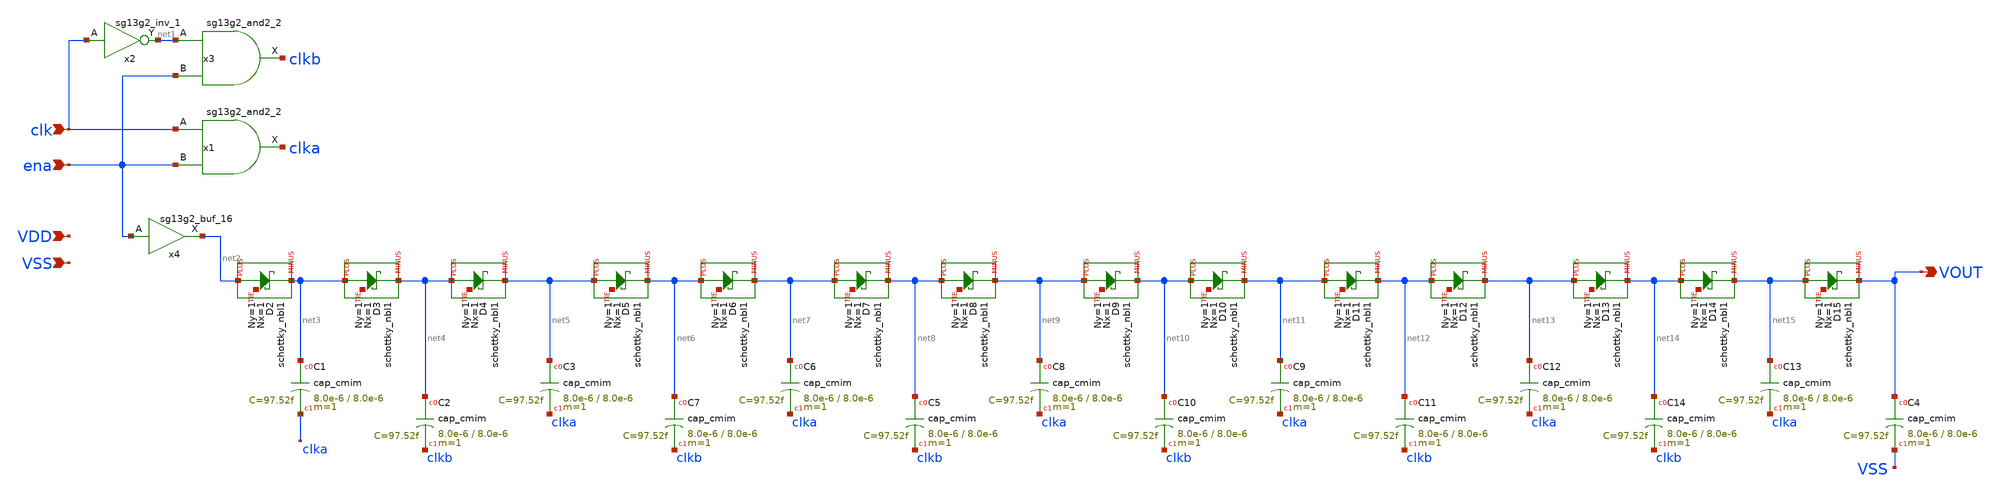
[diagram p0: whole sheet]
** sch_path: ihp130_cells/Schottky_PosChargePump/schottky_pump.sch
**.subckt schottky_pump clk ena VDD VSS VOUT
*.ipin clk
*.ipin ena
*.ipin VDD
*.ipin VSS
*.opin VOUT
XC1 net3 clka cap_cmim w=8.0e-6 l=8.0e-6 m=1 mm_ok=1
XC2 net4 clkb cap_cmim w=8.0e-6 l=8.0e-6 m=1 mm_ok=1
XC3 net5 clka cap_cmim w=8.0e-6 l=8.0e-6 m=1 mm_ok=1
XC4 VOUT VSS cap_cmim w=8.0e-6 l=8.0e-6 m=1 mm_ok=1
x1 clka clk ena VDD VSS sg13g2_and2_2
x2 net1 clk VDD VSS sg13g2_inv_1
x3 clkb net1 ena VDD VSS sg13g2_and2_2
x4 net2 ena VDD VSS sg13g2_buf_16
XC6 net7 clka cap_cmim w=8.0e-6 l=8.0e-6 m=1 mm_ok=1
XC7 net6 clkb cap_cmim w=8.0e-6 l=8.0e-6 m=1 mm_ok=1
XC5 net8 clkb cap_cmim w=8.0e-6 l=8.0e-6 m=1 mm_ok=1
XC8 net9 clka cap_cmim w=8.0e-6 l=8.0e-6 m=1 mm_ok=1
XC9 net11 clka cap_cmim w=8.0e-6 l=8.0e-6 m=1 mm_ok=1
XC10 net10 clkb cap_cmim w=8.0e-6 l=8.0e-6 m=1 mm_ok=1
XC11 net12 clkb cap_cmim w=8.0e-6 l=8.0e-6 m=1 mm_ok=1
XC12 net13 clka cap_cmim w=8.0e-6 l=8.0e-6 m=1 mm_ok=1
XC13 net15 clka cap_cmim w=8.0e-6 l=8.0e-6 m=1 mm_ok=1
XC14 net14 clkb cap_cmim w=8.0e-6 l=8.0e-6 m=1 mm_ok=1
XD2 net2 net3 net16 schottky_nbl1 Nx=1 Ny=1
XD3 net3 net4 net17 schottky_nbl1 Nx=1 Ny=1
XD4 net4 net5 net18 schottky_nbl1 Nx=1 Ny=1
XD5 net5 net6 net19 schottky_nbl1 Nx=1 Ny=1
XD6 net6 net7 net20 schottky_nbl1 Nx=1 Ny=1
XD7 net7 net8 net21 schottky_nbl1 Nx=1 Ny=1
XD8 net8 net9 net22 schottky_nbl1 Nx=1 Ny=1
XD9 net9 net10 net23 schottky_nbl1 Nx=1 Ny=1
XD10 net10 net11 net24 schottky_nbl1 Nx=1 Ny=1
XD11 net11 net12 net25 schottky_nbl1 Nx=1 Ny=1
XD12 net12 net13 net26 schottky_nbl1 Nx=1 Ny=1
XD13 net13 net14 net27 schottky_nbl1 Nx=1 Ny=1
XD14 net14 net15 net28 schottky_nbl1 Nx=1 Ny=1
XD15 net15 VOUT net29 schottky_nbl1 Nx=1 Ny=1
**.ends

* expanding   symbol:  sg13g2_stdcells/sg13g2_and2_2.sym # of pins=3
** sym_path: sg13g2_stdcells/sg13g2_and2_2.sym
** sch_path: sg13g2_stdcells/sg13g2_and2_2.sch
.subckt sg13g2_and2_2 X A B VDD VSS
*.ipin A
*.ipin B
*.opin X
*.iopin VDD
*.iopin VSS
XM1 net1 A net2 VSS sg13_lv_nmos w=640.00n l=130.00n ng=1 m=1 mm_ok=1
XM2 net2 B VSS VSS sg13_lv_nmos w=640.00n l=130.00n ng=1 m=1 mm_ok=1
XM3 X net1 VSS VSS sg13_lv_nmos w=1.48u l=130.00n ng=2 m=1 mm_ok=1
XM4 net1 B VDD VDD sg13_lv_pmos w=840.00n l=130.00n ng=1 m=1 mm_ok=1
XM5 net1 A VDD VDD sg13_lv_pmos w=840.00n l=130.00n ng=1 m=1 mm_ok=1
XM6 X net1 VDD VDD sg13_lv_pmos w=2.24u l=130.00n ng=2 m=1 mm_ok=1
.ends


* expanding   symbol:  sg13g2_stdcells/sg13g2_inv_1.sym # of pins=2
** sym_path: sg13g2_stdcells/sg13g2_inv_1.sym
** sch_path: sg13g2_stdcells/sg13g2_inv_1.sch
.subckt sg13g2_inv_1 Y A VDD VSS
*.opin Y
*.ipin A
*.iopin VDD
*.iopin VSS
XM1 Y A VSS VSS sg13_lv_nmos w=740.00n l=130.00n ng=1 m=1 mm_ok=1
XM2 Y A VDD VDD sg13_lv_pmos w=1.12u l=130.00n ng=1 m=1 mm_ok=1
.ends


* expanding   symbol:  sg13g2_stdcells/sg13g2_buf_16.sym # of pins=2
** sym_path: sg13g2_stdcells/sg13g2_buf_16.sym
** sch_path: sg13g2_stdcells/sg13g2_buf_16.sch
.subckt sg13g2_buf_16 X A VDD VSS
*.ipin A
*.opin X
*.iopin VDD
*.iopin VSS
XM1 net1 A VSS VSS sg13_lv_nmos w=4.44u l=130.00n ng=6 m=1 mm_ok=1
XM2 X net1 VSS VSS sg13_lv_nmos w=11.84u l=130.00n ng=16 m=1 mm_ok=1
XM3 net1 A VDD VDD sg13_lv_pmos w=6.72u l=130.00n ng=6 m=1 mm_ok=1
XM4 X net1 VDD VDD sg13_lv_pmos w=17.92u l=130.00n ng=16 m=1 mm_ok=1
.ends

.end
